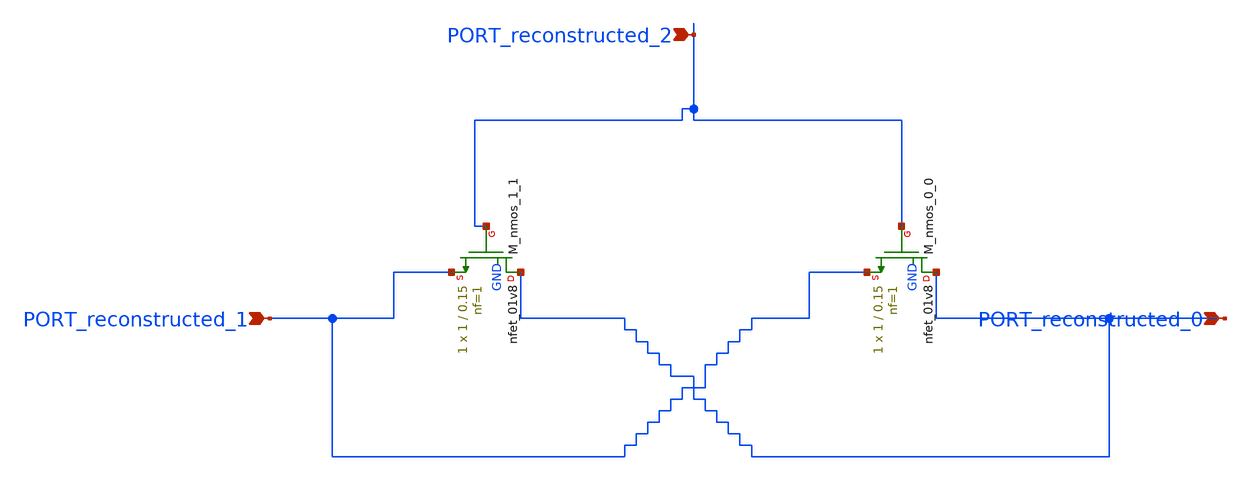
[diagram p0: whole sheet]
** sch_path: schematics/AMSNet/15.sch
**.subckt 15 PORT_reconstructed_2 PORT_reconstructed_0 PORT_reconstructed_1
*.ipin PORT_reconstructed_2
*.ipin PORT_reconstructed_0
*.ipin PORT_reconstructed_1
XM_nmos_0_0 PORT_reconstructed_0 PORT_reconstructed_2 PORT_reconstructed_1 GND sky130_fd_pr__nfet_01v8
+ L=0.15 W=1 nf=1 ad='int((1 + 1)/2) * 1 / 1 * 0.29' as='int((1 + 2)/2) * 1 / 1 * 0.29' pd='2*int((1 + 1)/2) * (1 / 1 + 0.29)'
+ ps='2*int((1 + 2)/2) * (1 / 1 + 0.29)' nrd='0.29 / 1 ' nrs='0.29 / 1 ' sa=0 sb=0 sd=0 mult=1 m=1
XM_nmos_1_1 PORT_reconstructed_0 PORT_reconstructed_2 PORT_reconstructed_1 GND sky130_fd_pr__nfet_01v8
+ L=0.15 W=1 nf=1 ad='int((1 + 1)/2) * 1 / 1 * 0.29' as='int((1 + 2)/2) * 1 / 1 * 0.29' pd='2*int((1 + 1)/2) * (1 / 1 + 0.29)'
+ ps='2*int((1 + 2)/2) * (1 / 1 + 0.29)' nrd='0.29 / 1 ' nrs='0.29 / 1 ' sa=0 sb=0 sd=0 mult=1 m=1
**.ends
.end
